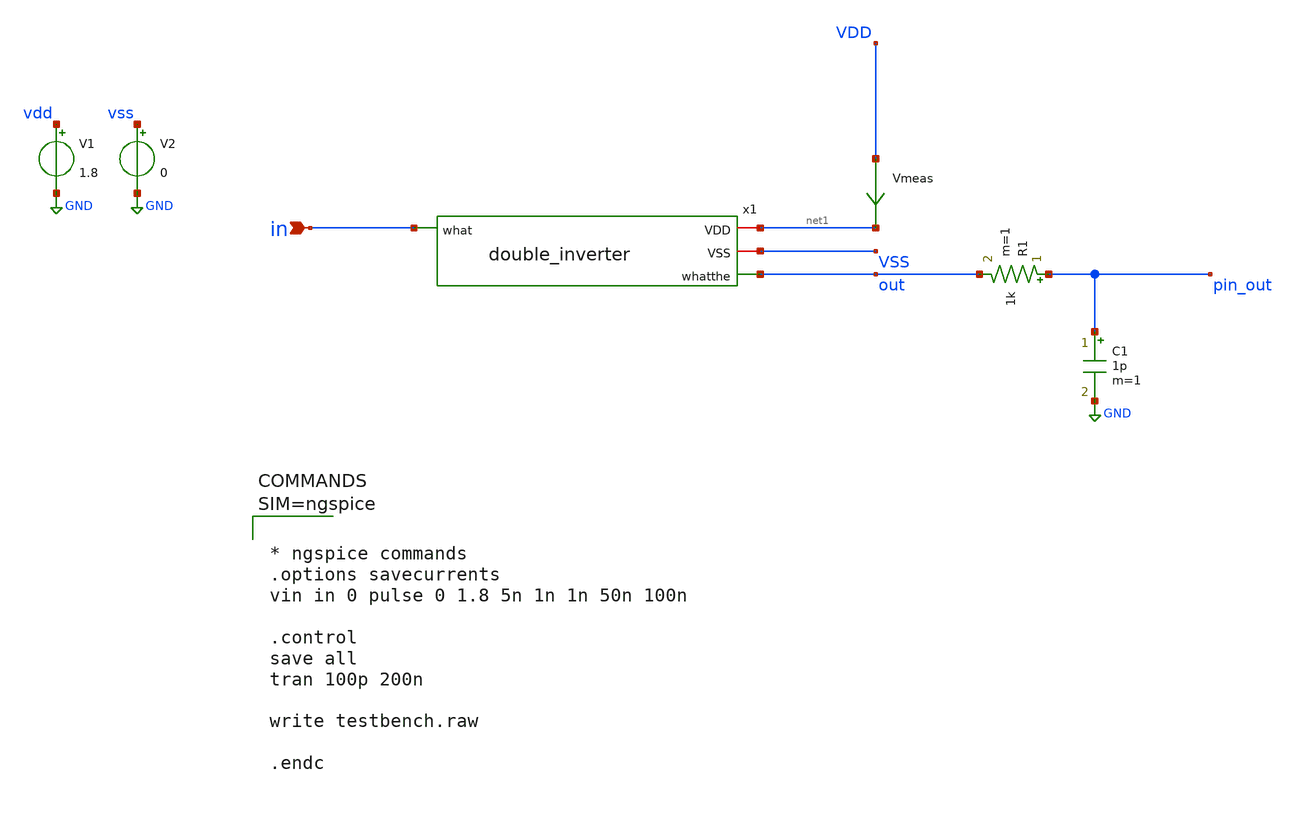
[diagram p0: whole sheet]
** sch_path: xschem/testbench.sch
**.subckt testbench in
*.ipin in
V1 vdd GND 1.8
V2 vss GND 0
x1 net1 VSS in out double_inverter
R1 pin_out out 1k m=1
C1 pin_out GND 1p m=1
Vmeas VDD net1 0
.save i(vmeas)
**** begin user architecture code

** opencircuitdesign pdks install
.lib $::SKYWATER_MODELS/sky130.lib.spice tt





* ngspice commands
.options savecurrents
vin in 0 pulse 0 1.8 5n 1n 1n 50n 100n

.control
save all
tran 100p 200n

write testbench.raw

.endc





**** end user architecture code
**.ends

* expanding   symbol:  double_inverter.sym # of pins=4
** sym_path: xschem/double_inverter.sym
** sch_path: xschem/double_inverter.sch
.subckt double_inverter VDD VSS what whatthe
*.iopin VDD
*.iopin VSS
*.ipin what
*.opin whatthe
XM1 inverted what VDD VDD sky130_fd_pr__pfet_01v8 L=0.15 W=1 nf=1 ad='int((nf+1)/2) * W/nf * 0.29' as='int((nf+2)/2) * W/nf * 0.29'
+ pd='2*int((nf+1)/2) * (W/nf + 0.29)' ps='2*int((nf+2)/2) * (W/nf + 0.29)' nrd='0.29 / W' nrs='0.29 / W'
+ sa=0 sb=0 sd=0 mult=1 m=1
XM2 inverted what VSS VSS sky130_fd_pr__nfet_01v8 L=0.15 W=1 nf=1 ad='int((nf+1)/2) * W/nf * 0.29' as='int((nf+2)/2) * W/nf * 0.29'
+ pd='2*int((nf+1)/2) * (W/nf + 0.29)' ps='2*int((nf+2)/2) * (W/nf + 0.29)' nrd='0.29 / W' nrs='0.29 / W'
+ sa=0 sb=0 sd=0 mult=1 m=1
XM3 whatthe inverted VDD VDD sky130_fd_pr__pfet_01v8 L=0.15 W=20 nf=20 ad='int((nf+1)/2) * W/nf * 0.29'
+ as='int((nf+2)/2) * W/nf * 0.29' pd='2*int((nf+1)/2) * (W/nf + 0.29)' ps='2*int((nf+2)/2) * (W/nf + 0.29)'
+ nrd='0.29 / W' nrs='0.29 / W' sa=0 sb=0 sd=0 mult=1 m=1
XM4 whatthe inverted VSS VSS sky130_fd_pr__nfet_01v8 L=0.15 W=20 nf=20 ad='int((nf+1)/2) * W/nf * 0.29'
+ as='int((nf+2)/2) * W/nf * 0.29' pd='2*int((nf+1)/2) * (W/nf + 0.29)' ps='2*int((nf+2)/2) * (W/nf + 0.29)'
+ nrd='0.29 / W' nrs='0.29 / W' sa=0 sb=0 sd=0 mult=1 m=1
.ends

.GLOBAL GND
.end
